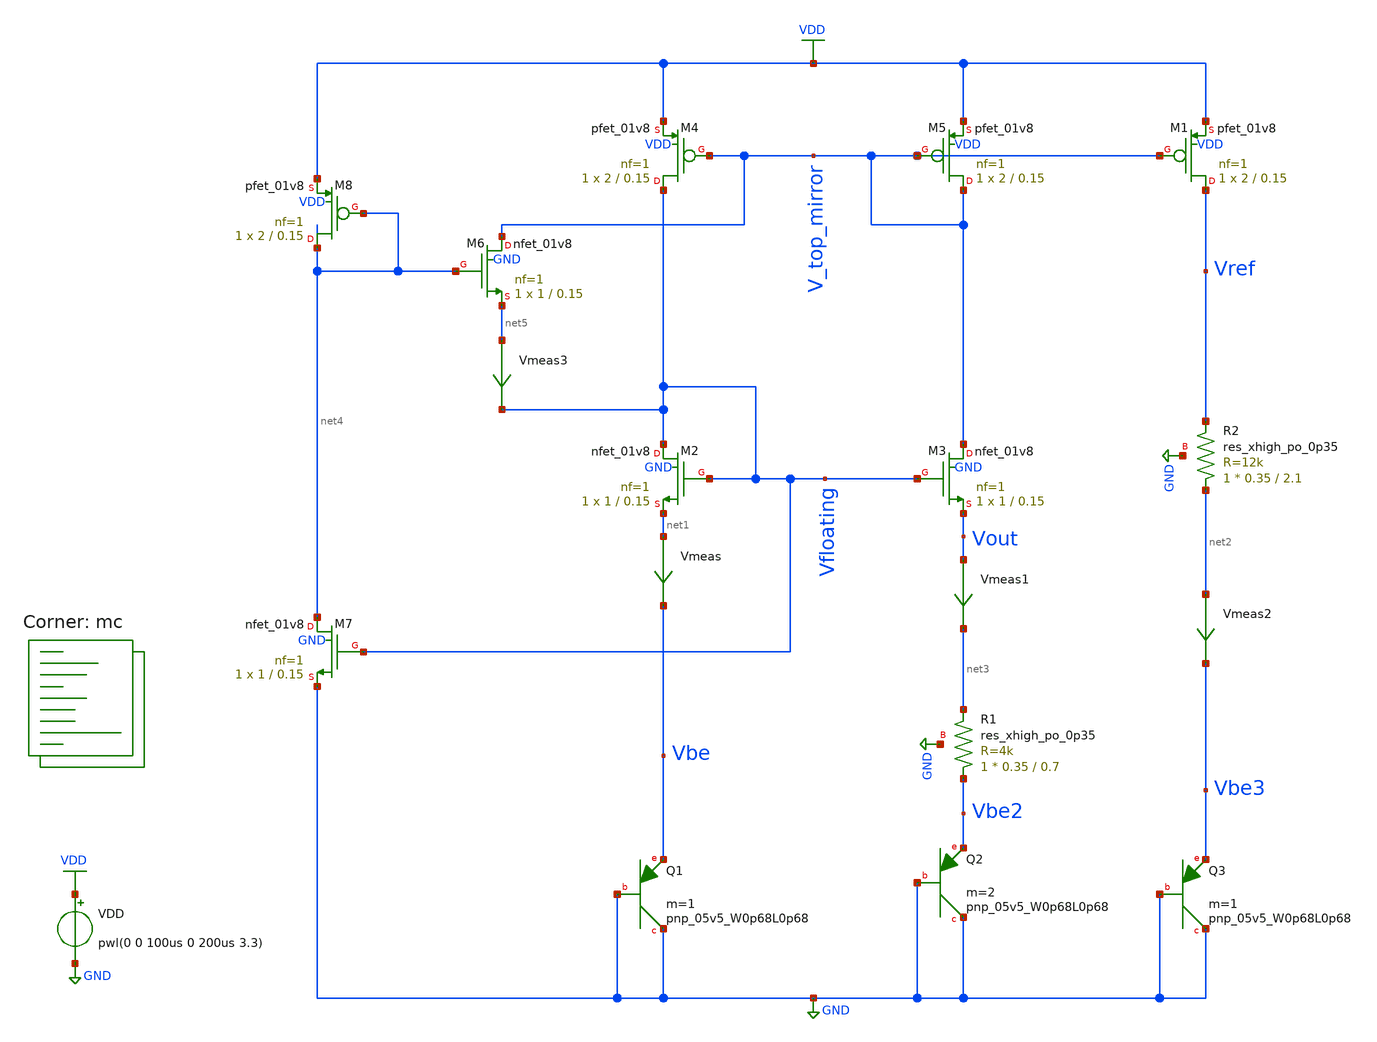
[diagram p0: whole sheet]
** sch_path: projects/pll/bandgapref/xschem_ngspice/mos_bandgap6.sch
**.subckt mos_bandgap6
XM2 Vfloating Vfloating net1 GND sky130_fd_pr__nfet_01v8 L=0.15 W=1 nf=1 ad='int((nf+1)/2) * W/nf * 0.29'
+ as='int((nf+2)/2) * W/nf * 0.29' pd='2*int((nf+1)/2) * (W/nf + 0.29)' ps='2*int((nf+2)/2) * (W/nf + 0.29)'
+ nrd='0.29 / W' nrs='0.29 / W' sa=0 sb=0 sd=0 mult=1 m=1
XM3 V_top_mirror Vfloating Vout GND sky130_fd_pr__nfet_01v8 L=0.15 W=1 nf=1 ad='int((nf+1)/2) * W/nf * 0.29'
+ as='int((nf+2)/2) * W/nf * 0.29' pd='2*int((nf+1)/2) * (W/nf + 0.29)' ps='2*int((nf+2)/2) * (W/nf + 0.29)'
+ nrd='0.29 / W' nrs='0.29 / W' sa=0 sb=0 sd=0 mult=1 m=1
XM4 Vfloating V_top_mirror VDD VDD sky130_fd_pr__pfet_01v8 L=0.15 W=2 nf=1 ad='int((nf+1)/2) * W/nf * 0.29'
+ as='int((nf+2)/2) * W/nf * 0.29' pd='2*int((nf+1)/2) * (W/nf + 0.29)' ps='2*int((nf+2)/2) * (W/nf + 0.29)'
+ nrd='0.29 / W' nrs='0.29 / W' sa=0 sb=0 sd=0 mult=1 m=1
XM5 V_top_mirror V_top_mirror VDD VDD sky130_fd_pr__pfet_01v8 L=0.15 W=2 nf=1 ad='int((nf+1)/2) * W/nf * 0.29'
+ as='int((nf+2)/2) * W/nf * 0.29' pd='2*int((nf+1)/2) * (W/nf + 0.29)' ps='2*int((nf+2)/2) * (W/nf + 0.29)'
+ nrd='0.29 / W' nrs='0.29 / W' sa=0 sb=0 sd=0 mult=1 m=1
VDD VDD GND pwl(0 0 100us 0 200us 3.3)
Vmeas net1 Vbe 0
.save i(vmeas)
Vmeas1 Vout net3 0
.save i(vmeas1)
Vmeas2 net2 Vbe3 0
.save i(vmeas2)
XM1 Vref V_top_mirror VDD VDD sky130_fd_pr__pfet_01v8 L=0.15 W=2 nf=1 ad='int((nf+1)/2) * W/nf * 0.29'
+ as='int((nf+2)/2) * W/nf * 0.29' pd='2*int((nf+1)/2) * (W/nf + 0.29)' ps='2*int((nf+2)/2) * (W/nf + 0.29)'
+ nrd='0.29 / W' nrs='0.29 / W' sa=0 sb=0 sd=0 mult=1 m=1
XR1 Vbe2 net3 GND sky130_fd_pr__res_xhigh_po_0p35 L=0.7 mult=1 m=1
XQ1 GND GND Vbe sky130_fd_pr__pnp_05v5_W0p68L0p68 m=1
XQ2 GND GND Vbe2 sky130_fd_pr__pnp_05v5_W0p68L0p68 m=2
XQ3 GND GND Vbe3 sky130_fd_pr__pnp_05v5_W0p68L0p68 m=1
XM6 V_top_mirror net4 net5 GND sky130_fd_pr__nfet_01v8 L=0.15 W=1 nf=1 ad='int((nf+1)/2) * W/nf * 0.29'
+ as='int((nf+2)/2) * W/nf * 0.29' pd='2*int((nf+1)/2) * (W/nf + 0.29)' ps='2*int((nf+2)/2) * (W/nf + 0.29)'
+ nrd='0.29 / W' nrs='0.29 / W' sa=0 sb=0 sd=0 mult=1 m=1
XM7 net4 Vfloating GND GND sky130_fd_pr__nfet_01v8 L=0.15 W=1 nf=1 ad='int((nf+1)/2) * W/nf * 0.29' as='int((nf+2)/2) * W/nf * 0.29'
+ pd='2*int((nf+1)/2) * (W/nf + 0.29)' ps='2*int((nf+2)/2) * (W/nf + 0.29)' nrd='0.29 / W' nrs='0.29 / W'
+ sa=0 sb=0 sd=0 mult=1 m=1
XM8 net4 net4 VDD VDD sky130_fd_pr__pfet_01v8 L=0.15 W=2 nf=1 ad='int((nf+1)/2) * W/nf * 0.29' as='int((nf+2)/2) * W/nf * 0.29'
+ pd='2*int((nf+1)/2) * (W/nf + 0.29)' ps='2*int((nf+2)/2) * (W/nf + 0.29)' nrd='0.29 / W' nrs='0.29 / W'
+ sa=0 sb=0 sd=0 mult=1 m=1
XR2 net2 Vref GND sky130_fd_pr__res_xhigh_po_0p35 L=2.1 mult=1 m=1
Vmeas3 net5 Vfloating 0
.save i(vmeas3)
**** begin user architecture code
.lib $::SKYWATER_MODELS/sky130.lib.spice mc



.option method=gear
.option wnflag=1
.option savecurrents

*  .param VDDGAUSS = agauss(3.3, 0.05, 1)
*  .param VDD = VDDGAUSS
** use following line to remove VCC variations
* .param VDD = 3.3

.control
save all
op
tran 20ns 500us
remzerovec
write mos_bandgap6.raw
set appendwrite
.endc



**** end user architecture code
**.ends
.GLOBAL GND
.GLOBAL VDD
.end
